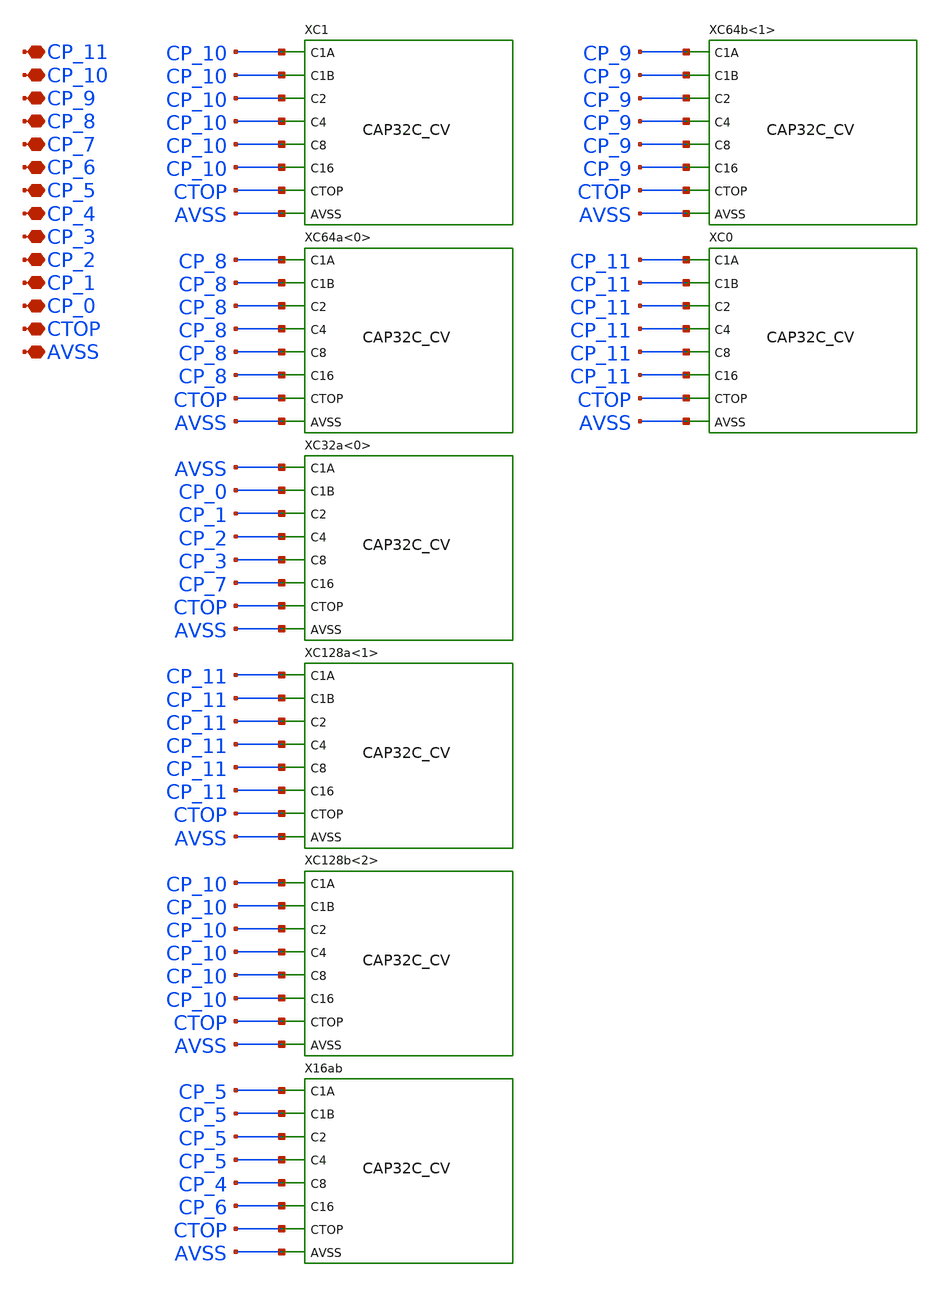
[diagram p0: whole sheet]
** sch_path: sim/SAR9B/build/SUN_SAR9B_SK130NM/xschem/SUN_SAR9B_SK130NM/CDAC8_CV.sch
**.subckt CDAC8_CV CP_11 CP_10 CP_9 CP_8 CP_7 CP_6 CP_5 CP_4 CP_3 CP_2 CP_1 CP_0 CTOP AVSS
*.iopin CP_11
*.iopin CP_10
*.iopin CP_9
*.iopin CP_8
*.iopin CP_7
*.iopin CP_6
*.iopin CP_5
*.iopin CP_4
*.iopin CP_3
*.iopin CP_2
*.iopin CP_1
*.iopin CP_0
*.iopin CTOP
*.iopin AVSS
XC1 CP_10 CP_10 CP_10 CP_10 CP_10 CP_10 CTOP AVSS CAP32C_CV
XC64a<0> CP_8 CP_8 CP_8 CP_8 CP_8 CP_8 CTOP AVSS CAP32C_CV
XC32a<0> AVSS CP_0 CP_1 CP_2 CP_3 CP_7 CTOP AVSS CAP32C_CV
XC128a<1> CP_11 CP_11 CP_11 CP_11 CP_11 CP_11 CTOP AVSS CAP32C_CV
XC128b<2> CP_10 CP_10 CP_10 CP_10 CP_10 CP_10 CTOP AVSS CAP32C_CV
X16ab CP_5 CP_5 CP_5 CP_5 CP_4 CP_6 CTOP AVSS CAP32C_CV
XC64b<1> CP_9 CP_9 CP_9 CP_9 CP_9 CP_9 CTOP AVSS CAP32C_CV
XC0 CP_11 CP_11 CP_11 CP_11 CP_11 CP_11 CTOP AVSS CAP32C_CV
**.ends
.end
